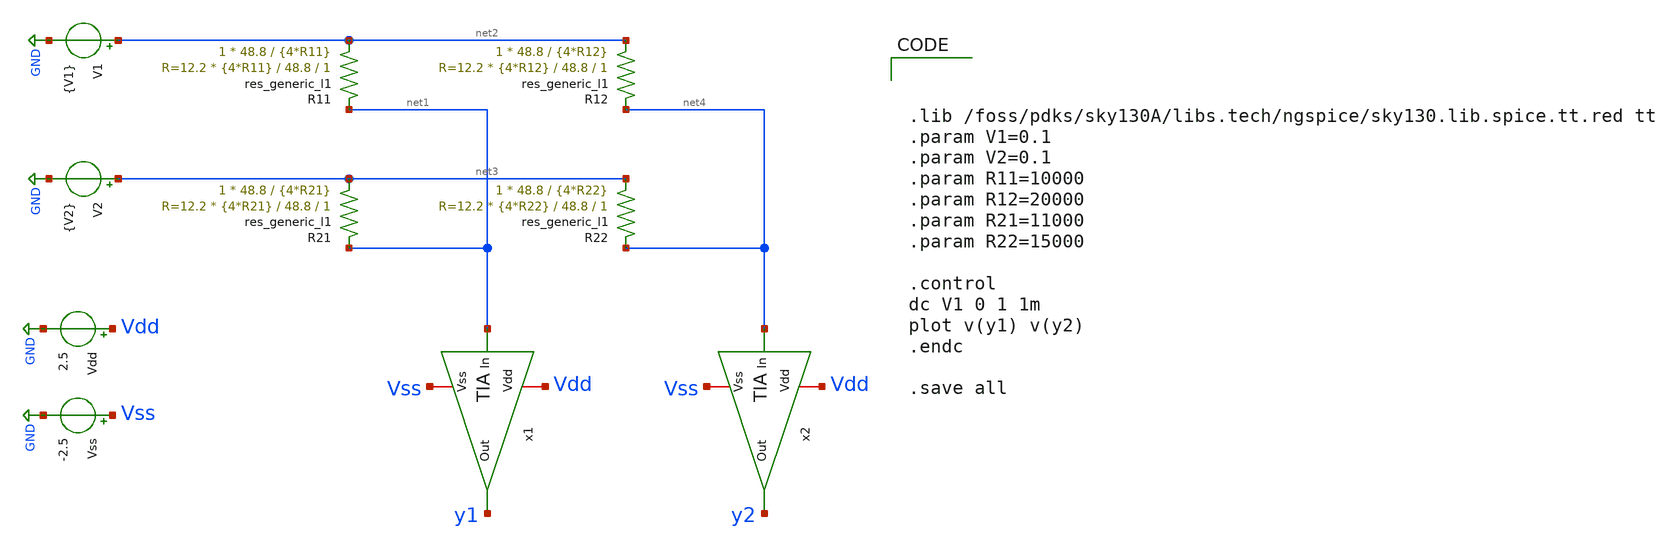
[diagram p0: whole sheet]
** sch_path: Vector-Matrix-Multiplicaction/xschem/VMM.sch
**.subckt VMM
x1 Vdd net1 y1 Vss TIA
R11 net2 net1 sky130_fd_pr__res_generic_l1 W=48.8 L={4*R11} m=1
R12 net2 net4 sky130_fd_pr__res_generic_l1 W=48.8 L={4*R12} m=1
R21 net3 net1 sky130_fd_pr__res_generic_l1 W=48.8 L={4*R21} m=1
R22 net3 net4 sky130_fd_pr__res_generic_l1 W=48.8 L={4*R22} m=1
x2 Vdd net4 y2 Vss TIA
Vdd Vdd GND 2.5
Vss Vss GND -2.5
V1 net2 GND {V1}
V2 net3 GND {V2}
**** begin user architecture code



.lib /foss/pdks/sky130A/libs.tech/ngspice/sky130.lib.spice.tt.red tt
.param V1=0.1
.param V2=0.1
.param R11=10000
.param R12=20000
.param R21=11000
.param R22=15000

.control
dc V1 0 1 1m
plot v(y1) v(y2)
.endc

.save all



**** end user architecture code
**.ends

* expanding   symbol:  /foss/designs/ProyectoChipUSM/TIA.sym # of pins=4
** sym_path: Vector-Matrix-Multiplicaction/xschem/TIA.sym
** sch_path: Vector-Matrix-Multiplicaction/xschem/TIA.sch
.subckt TIA Vdd In Out Vss
*.ipin In
*.opin Out
*.iopin Vdd
*.iopin Vss
Rf1 In Out sky130_fd_pr__res_generic_l1 W=48.8 L=20000 m=1
XMp Out In Vdd Vdd sky130_fd_pr__pfet_g5v0d10v5 L=1 W=15 nf=1 ad='int((nf+1)/2) * W/nf * 0.29' as='int((nf+2)/2) * W/nf * 0.29'
+ pd='2*int((nf+1)/2) * (W/nf + 0.29)' ps='2*int((nf+2)/2) * (W/nf + 0.29)' nrd='0.29 / W' nrs='0.29 / W'
+ sa=0 sb=0 sd=0 mult=1 m=1
XMn Out In Vss Vss sky130_fd_pr__nfet_g5v0d10v5 L=1 W=5 nf=1 ad='int((nf+1)/2) * W/nf * 0.29' as='int((nf+2)/2) * W/nf * 0.29'
+ pd='2*int((nf+1)/2) * (W/nf + 0.29)' ps='2*int((nf+2)/2) * (W/nf + 0.29)' nrd='0.29 / W' nrs='0.29 / W'
+ sa=0 sb=0 sd=0 mult=1 m=1
.ends

.GLOBAL GND
.end
